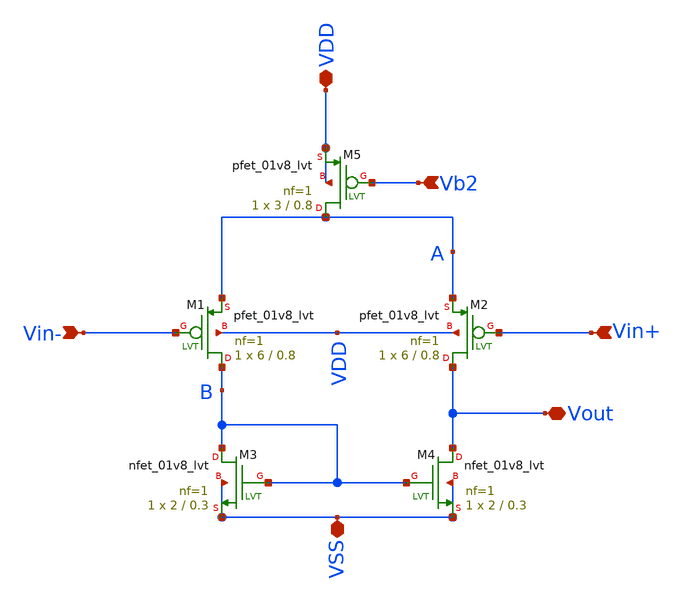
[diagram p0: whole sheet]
** sch_path: xschem/Amplifiers/VA5.sch
**.subckt VA5 Vin+ Vin- Vout Vb2 VDD VSS
*.ipin Vin+
*.ipin Vin-
*.iopin Vout
*.ipin Vb2
*.iopin VDD
*.iopin VSS
XM1 B Vin- A VDD sky130_fd_pr__pfet_01v8_lvt L=0.8 W=6 nf=1 ad='int((nf+1)/2) * W/nf * 0.29' as='int((nf+2)/2) * W/nf * 0.29'
+ pd='2*int((nf+1)/2) * (W/nf + 0.29)' ps='2*int((nf+2)/2) * (W/nf + 0.29)' nrd='0.29 / W' nrs='0.29 / W'
+ sa=0 sb=0 sd=0 mult=1 m=1
XM2 Vout Vin+ A VDD sky130_fd_pr__pfet_01v8_lvt L=0.8 W=6 nf=1 ad='int((nf+1)/2) * W/nf * 0.29' as='int((nf+2)/2) * W/nf * 0.29'
+ pd='2*int((nf+1)/2) * (W/nf + 0.29)' ps='2*int((nf+2)/2) * (W/nf + 0.29)' nrd='0.29 / W' nrs='0.29 / W'
+ sa=0 sb=0 sd=0 mult=1 m=1
XM5 A Vb2 VDD VDD sky130_fd_pr__pfet_01v8_lvt L=0.8 W=3 nf=1 ad='int((nf+1)/2) * W/nf * 0.29' as='int((nf+2)/2) * W/nf * 0.29'
+ pd='2*int((nf+1)/2) * (W/nf + 0.29)' ps='2*int((nf+2)/2) * (W/nf + 0.29)' nrd='0.29 / W' nrs='0.29 / W'
+ sa=0 sb=0 sd=0 mult=1 m=1
XM3 B B VSS VSS sky130_fd_pr__nfet_01v8_lvt L=0.3 W=2 nf=1 ad='int((nf+1)/2) * W/nf * 0.29' as='int((nf+2)/2) * W/nf * 0.29'
+ pd='2*int((nf+1)/2) * (W/nf + 0.29)' ps='2*int((nf+2)/2) * (W/nf + 0.29)' nrd='0.29 / W' nrs='0.29 / W'
+ sa=0 sb=0 sd=0 mult=1 m=1
XM4 Vout B VSS VSS sky130_fd_pr__nfet_01v8_lvt L=0.3 W=2 nf=1 ad='int((nf+1)/2) * W/nf * 0.29' as='int((nf+2)/2) * W/nf * 0.29'
+ pd='2*int((nf+1)/2) * (W/nf + 0.29)' ps='2*int((nf+2)/2) * (W/nf + 0.29)' nrd='0.29 / W' nrs='0.29 / W'
+ sa=0 sb=0 sd=0 mult=1 m=1
**.ends
.end
